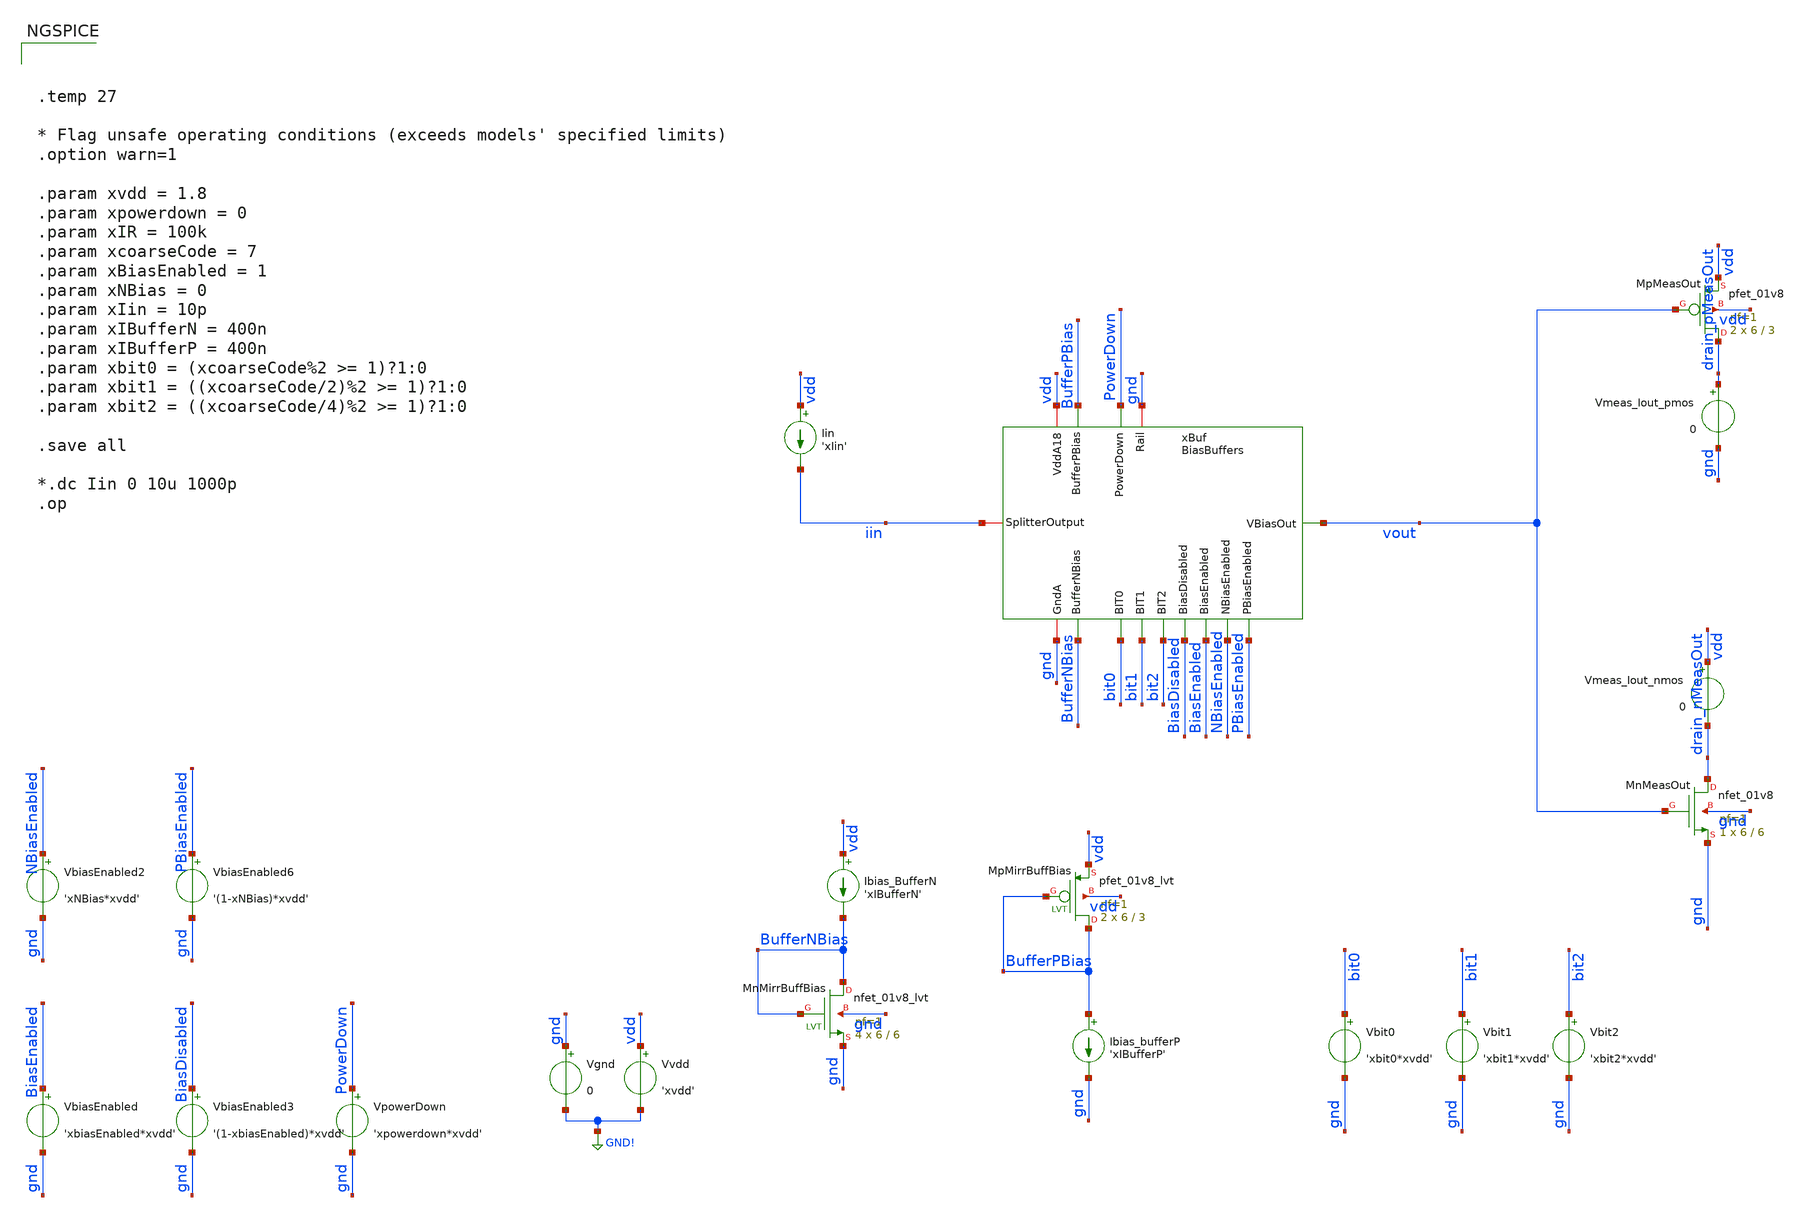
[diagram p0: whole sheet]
** sch_path: analog/xschem/tb_BiasBuffers.sch
**.subckt tb_BiasBuffers
Vgnd gnd GND! 0
.save i(vgnd)
Vvdd vdd GND! 'xvdd'
.save i(vvdd)
VpowerDown PowerDown gnd 'xpowerdown*xvdd'
.save i(vpowerdown)
Vbit0 bit0 gnd 'xbit0*xvdd'
.save i(vbit0)
Vbit1 bit1 gnd 'xbit1*xvdd'
.save i(vbit1)
Vbit2 bit2 gnd 'xbit2*xvdd'
.save i(vbit2)
xBuf vdd gnd BufferNBias iin bit0 bit1 bit2 BiasDisabled BiasEnabled NBiasEnabled PBiasEnabled
+ BufferPBias PowerDown gnd vout BiasBuffers
Iin vdd iin 'xIin'
XMnMeasOut drain_nMeasOut vout gnd gnd sky130_fd_pr__nfet_01v8 L=6 W=6 nf=1 ad='int((1 + 1)/2) * 6 / 1 * 0.29'
+ as='int((1 + 2)/2) * 6 / 1 * 0.29' pd='2*int((1 + 1)/2) * (6 / 1 + 0.29)' ps='2*int((1 + 2)/2) * (6 / 1 + 0.29)'
+ nrd='0.29 / 6 ' nrs='0.29 / 6 ' sa=0 sb=0 sd=0 mult=1 m=1
Vmeas_Iout_nmos vdd drain_nMeasOut 0
.save i(vmeas_iout_nmos)
XMpMeasOut drain_pMeasOut vout vdd vdd sky130_fd_pr__pfet_01v8 L=3 W=6 nf=1 ad='int((1 + 1)/2) * 6 / 1 * 0.29'
+ as='int((1 + 2)/2) * 6 / 1 * 0.29' pd='2*int((1 + 1)/2) * (6 / 1 + 0.29)' ps='2*int((1 + 2)/2) * (6 / 1 + 0.29)'
+ nrd='0.29 / 6 ' nrs='0.29 / 6 ' sa=0 sb=0 sd=0 mult=2 m=2
Vmeas_Iout_pmos drain_pMeasOut gnd 0
.save i(vmeas_iout_pmos)
XMnMirrBuffBias BufferNBias BufferNBias gnd gnd sky130_fd_pr__nfet_01v8_lvt L=6 W=6 nf=1 ad='int((1 + 1)/2) * 6 / 1 * 0.29'
+ as='int((1 + 2)/2) * 6 / 1 * 0.29' pd='2*int((1 + 1)/2) * (6 / 1 + 0.29)' ps='2*int((1 + 2)/2) * (6 / 1 + 0.29)'
+ nrd='0.29 / 6 ' nrs='0.29 / 6 ' sa=0 sb=0 sd=0 mult=4 m=4
Ibias_BufferN vdd BufferNBias 'xIBufferN'
XMpMirrBuffBias BufferPBias BufferPBias vdd vdd sky130_fd_pr__pfet_01v8_lvt L=3 W=6 nf=1 ad='int((1 + 1)/2) * 6 / 1 * 0.29'
+ as='int((1 + 2)/2) * 6 / 1 * 0.29' pd='2*int((1 + 1)/2) * (6 / 1 + 0.29)' ps='2*int((1 + 2)/2) * (6 / 1 + 0.29)'
+ nrd='0.29 / 6 ' nrs='0.29 / 6 ' sa=0 sb=0 sd=0 mult=2 m=2
Ibias_bufferP BufferPBias gnd 'xIBufferP'
VbiasEnabled BiasEnabled gnd 'xbiasEnabled*xvdd'
VbiasEnabled3 BiasDisabled gnd '(1-xbiasEnabled)*xvdd'
VbiasEnabled2 NBiasEnabled gnd 'xNBias*xvdd'
VbiasEnabled6 PBiasEnabled gnd '(1-xNBias)*xvdd'
**** begin user architecture code

** opencircuitdesign pdks install
.lib $::SKYWATER_MODELS/sky130.lib.spice tt




.temp 27

* Flag unsafe operating conditions (exceeds models' specified limits)
.option warn=1

.param xvdd = 1.8
.param xpowerdown = 0
.param xIR = 100k
.param xcoarseCode = 7
.param xBiasEnabled = 1
.param xNBias = 0
.param xIin = 10p
.param xIBufferN = 400n
.param xIBufferP = 400n
.param xbit0 = (xcoarseCode%2 >= 1)?1:0
.param xbit1 = ((xcoarseCode/2)%2 >= 1)?1:0
.param xbit2 = ((xcoarseCode/4)%2 >= 1)?1:0

.save all

*.dc Iin 0 10u 1000p
.op


**** end user architecture code
**.ends
.GLOBAL GND!
.end
